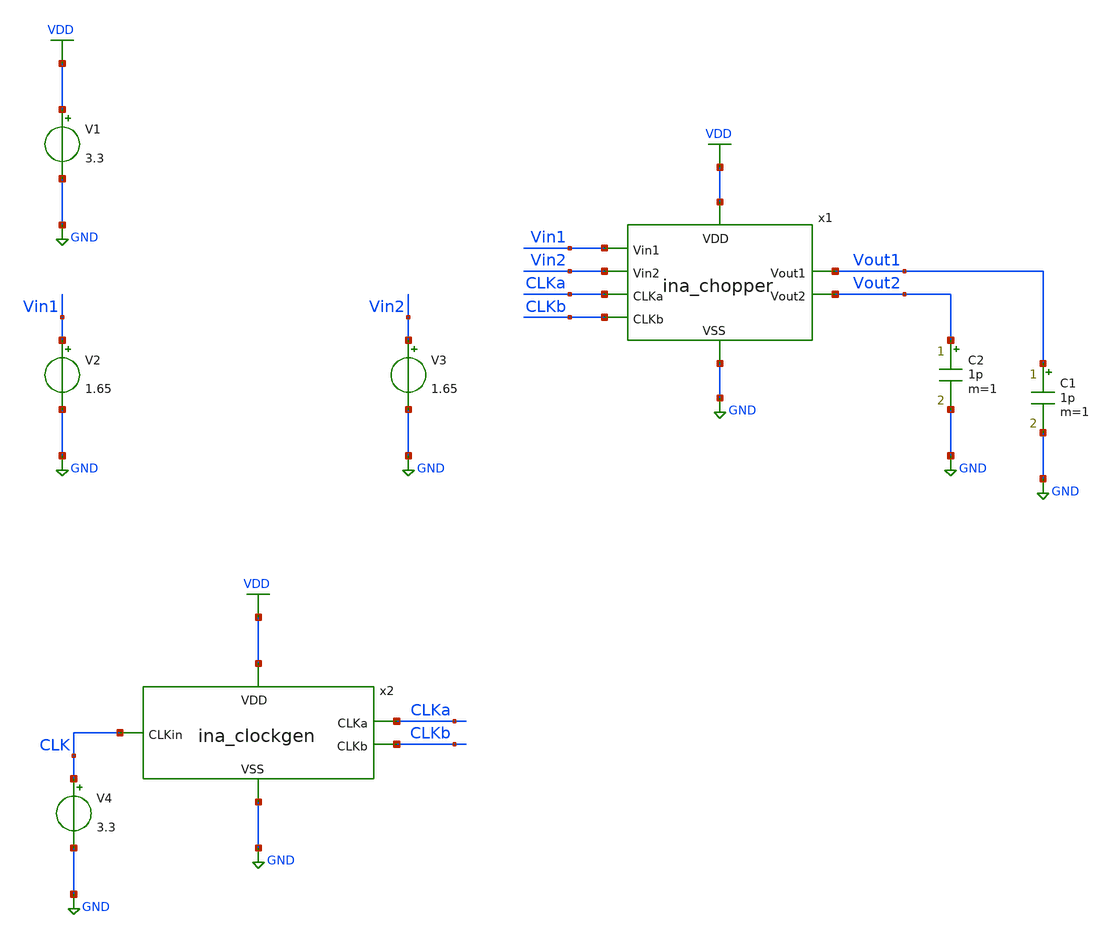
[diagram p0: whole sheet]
** sch_path: designs/libs/tb_ina/tb_ina_chopper_tran/tb_ina_chopper_tran.sch
**.subckt tb_ina_chopper_tran
V1 VDD GND 3.3
V2 Vin1 GND 1.65
V4 CLK GND 3.3
V3 Vin2 GND 1.65
C2 Vout2 GND 1p m=1
C1 Vout1 GND 1p m=1
x1 Vout2 Vin1 VDD GND CLKb CLKa Vout1 Vin2 ina_chopper
x2 VDD CLK CLKa CLKb GND ina_clockgen
**** begin user architecture code

.include $::180MCU_MODELS/design.ngspice
.lib $::180MCU_MODELS/sm141064.ngspice typical
.lib $::180MCU_MODELS/sm141064.ngspice cap_mim
.lib $::180MCU_MODELS/sm141064.ngspice moscap_typical
.lib $::180MCU_MODELS/sm141064.ngspice mimcap_typical
.lib $::180MCU_MODELS/sm141064.ngspice res_typical
* .lib $::180MCU_MODELS/sm141064.ngspice res_statistical
* ngspice commands




.control
save all

run
set color0 = white

*************************************
** ECG INPUT PARAMETERS
*************************************

let Vdd  = 3.3
let Vcm  = 1.65
let Vamp = 0.5m
let fecg = 100

*************************************
** CHOPPER PARAMETERS
*************************************

let fchop = 4k
let tper = 1/fchop
let ton = tper/2
let tr = 10n
let tf = 10n

*************************************
** TRANSIENT PARAMETERS
*************************************

let tstop = 10m
let tstep = 100n

*************************************
** SOURCES
*************************************

alter @V1[DC] = $&Vdd
alter @V2[SIN] = [ $&Vcm $&Vamp $&fecg ]
alter @V3[SIN] = [ $&Vcm -$&Vamp $&fecg ]
alter @V4[PULSE] = [ 0 $&Vdd 0 $&tr $&tf $&ton $&tper 0 ]

*************************************
** TRANSIENT SIMULATION
*************************************

tran $&tstep $&tstop

*************************************
** PLOTS
*************************************

setplot tran1
let vin_diff  = v(Vin1)-v(Vin2)
let vout_diff = v(Vout1)-v(Vout2)
let vin1 = v(Vin1)
let vin2 = v(Vin2)
let vout1 = v(Vout1)
let vout2 = v(Vout2)
let vclka = v(CLKa)
let vclkb = v(CLKb)
meas tran vmax1 MAX v(Vout1)
meas tran vmin1 MIN v(Vout1)
let spike = ((vmax1-vmin1)-1m)/2
plot vin_diff
plot vout_diff
plot vin1 vin2
plot vclka vclkb xlimit 0 500u
plot vout1 vout2
print spike

*************************************
** SAVE
*************************************

write tb_ina_chopper_tran.raw


.endc
* ngspice commands



**** end user architecture code
**.ends

* expanding   symbol:  libs/core_ina/ina_chopper/ina_chopper.sym # of pins=8
** sym_path: designs/libs/core_ina/ina_chopper/ina_chopper.sym
** sch_path: designs/libs/core_ina/ina_chopper/ina_chopper.sch
.subckt ina_chopper Vout2 Vin1 VDD VSS CLKb CLKa Vout1 Vin2
*.ipin Vin1
*.ipin Vin2
*.ipin CLKb
*.opin Vout2
*.ipin CLKa
*.opin Vout1
*.ipin VDD
*.ipin VSS
XM1 Vout1 CLKa Vin1 VSS nfet_03v3 L=0.28u W=2u nf=1 ad='int((nf+1)/2) * W/nf * 0.18u' as='int((nf+2)/2) * W/nf * 0.18u'
+ pd='2*int((nf+1)/2) * (W/nf + 0.18u)' ps='2*int((nf+2)/2) * (W/nf + 0.18u)' nrd='0.18u / W' nrs='0.18u / W'
+ sa=0 sb=0 sd=0 m=1
XM2 Vout1 CLKb Vin1 VDD pfet_03v3 L=0.28u W=2u nf=1 ad='int((nf+1)/2) * W/nf * 0.18u' as='int((nf+2)/2) * W/nf * 0.18u'
+ pd='2*int((nf+1)/2) * (W/nf + 0.18u)' ps='2*int((nf+2)/2) * (W/nf + 0.18u)' nrd='0.18u / W' nrs='0.18u / W'
+ sa=0 sb=0 sd=0 m=2
XM3 Vout2 CLKb Vin1 VSS nfet_03v3 L=0.28u W=2u nf=1 ad='int((nf+1)/2) * W/nf * 0.18u' as='int((nf+2)/2) * W/nf * 0.18u'
+ pd='2*int((nf+1)/2) * (W/nf + 0.18u)' ps='2*int((nf+2)/2) * (W/nf + 0.18u)' nrd='0.18u / W' nrs='0.18u / W'
+ sa=0 sb=0 sd=0 m=1
XM4 Vout2 CLKa Vin1 VDD pfet_03v3 L=0.28u W=2u nf=1 ad='int((nf+1)/2) * W/nf * 0.18u' as='int((nf+2)/2) * W/nf * 0.18u'
+ pd='2*int((nf+1)/2) * (W/nf + 0.18u)' ps='2*int((nf+2)/2) * (W/nf + 0.18u)' nrd='0.18u / W' nrs='0.18u / W'
+ sa=0 sb=0 sd=0 m=2
XM5 Vin2 CLKa Vout2 VSS nfet_03v3 L=0.28u W=2u nf=1 ad='int((nf+1)/2) * W/nf * 0.18u' as='int((nf+2)/2) * W/nf * 0.18u'
+ pd='2*int((nf+1)/2) * (W/nf + 0.18u)' ps='2*int((nf+2)/2) * (W/nf + 0.18u)' nrd='0.18u / W' nrs='0.18u / W'
+ sa=0 sb=0 sd=0 m=1
XM6 Vin2 CLKb Vout2 VDD pfet_03v3 L=0.28u W=2u nf=1 ad='int((nf+1)/2) * W/nf * 0.18u' as='int((nf+2)/2) * W/nf * 0.18u'
+ pd='2*int((nf+1)/2) * (W/nf + 0.18u)' ps='2*int((nf+2)/2) * (W/nf + 0.18u)' nrd='0.18u / W' nrs='0.18u / W'
+ sa=0 sb=0 sd=0 m=2
XM7 Vin2 CLKb Vout1 VSS nfet_03v3 L=0.28u W=2u nf=1 ad='int((nf+1)/2) * W/nf * 0.18u' as='int((nf+2)/2) * W/nf * 0.18u'
+ pd='2*int((nf+1)/2) * (W/nf + 0.18u)' ps='2*int((nf+2)/2) * (W/nf + 0.18u)' nrd='0.18u / W' nrs='0.18u / W'
+ sa=0 sb=0 sd=0 m=1
XM8 Vin2 CLKa Vout1 VDD pfet_03v3 L=0.28u W=2u nf=1 ad='int((nf+1)/2) * W/nf * 0.18u' as='int((nf+2)/2) * W/nf * 0.18u'
+ pd='2*int((nf+1)/2) * (W/nf + 0.18u)' ps='2*int((nf+2)/2) * (W/nf + 0.18u)' nrd='0.18u / W' nrs='0.18u / W'
+ sa=0 sb=0 sd=0 m=2
XM9 Vout1 CLKb Vout1 VSS nfet_03v3 L=0.28u W=1u nf=1 ad='int((nf+1)/2) * W/nf * 0.18u' as='int((nf+2)/2) * W/nf * 0.18u'
+ pd='2*int((nf+1)/2) * (W/nf + 0.18u)' ps='2*int((nf+2)/2) * (W/nf + 0.18u)' nrd='0.18u / W' nrs='0.18u / W'
+ sa=0 sb=0 sd=0 m=1
XM10 Vout1 CLKa Vout1 VDD pfet_03v3 L=0.28u W=1u nf=1 ad='int((nf+1)/2) * W/nf * 0.18u' as='int((nf+2)/2) * W/nf * 0.18u'
+ pd='2*int((nf+1)/2) * (W/nf + 0.18u)' ps='2*int((nf+2)/2) * (W/nf + 0.18u)' nrd='0.18u / W' nrs='0.18u / W'
+ sa=0 sb=0 sd=0 m=2
XM11 Vout2 CLKa Vout2 VSS nfet_03v3 L=0.28u W=1u nf=1 ad='int((nf+1)/2) * W/nf * 0.18u' as='int((nf+2)/2) * W/nf * 0.18u'
+ pd='2*int((nf+1)/2) * (W/nf + 0.18u)' ps='2*int((nf+2)/2) * (W/nf + 0.18u)' nrd='0.18u / W' nrs='0.18u / W'
+ sa=0 sb=0 sd=0 m=1
XM12 Vout2 CLKb Vout2 VDD pfet_03v3 L=0.28u W=1u nf=1 ad='int((nf+1)/2) * W/nf * 0.18u' as='int((nf+2)/2) * W/nf * 0.18u'
+ pd='2*int((nf+1)/2) * (W/nf + 0.18u)' ps='2*int((nf+2)/2) * (W/nf + 0.18u)' nrd='0.18u / W' nrs='0.18u / W'
+ sa=0 sb=0 sd=0 m=2
XM13 Vout2 CLKa Vout2 VDD pfet_03v3 L=0.28u W=1u nf=1 ad='int((nf+1)/2) * W/nf * 0.18u' as='int((nf+2)/2) * W/nf * 0.18u'
+ pd='2*int((nf+1)/2) * (W/nf + 0.18u)' ps='2*int((nf+2)/2) * (W/nf + 0.18u)' nrd='0.18u / W' nrs='0.18u / W'
+ sa=0 sb=0 sd=0 m=2
XM14 Vout2 CLKb Vout2 VSS nfet_03v3 L=0.28u W=1u nf=1 ad='int((nf+1)/2) * W/nf * 0.18u' as='int((nf+2)/2) * W/nf * 0.18u'
+ pd='2*int((nf+1)/2) * (W/nf + 0.18u)' ps='2*int((nf+2)/2) * (W/nf + 0.18u)' nrd='0.18u / W' nrs='0.18u / W'
+ sa=0 sb=0 sd=0 m=1
XM15 Vout1 CLKb Vout1 VDD pfet_03v3 L=0.28u W=1u nf=1 ad='int((nf+1)/2) * W/nf * 0.18u' as='int((nf+2)/2) * W/nf * 0.18u'
+ pd='2*int((nf+1)/2) * (W/nf + 0.18u)' ps='2*int((nf+2)/2) * (W/nf + 0.18u)' nrd='0.18u / W' nrs='0.18u / W'
+ sa=0 sb=0 sd=0 m=2
XM16 Vout1 CLKa Vout1 VSS nfet_03v3 L=0.28u W=1u nf=1 ad='int((nf+1)/2) * W/nf * 0.18u' as='int((nf+2)/2) * W/nf * 0.18u'
+ pd='2*int((nf+1)/2) * (W/nf + 0.18u)' ps='2*int((nf+2)/2) * (W/nf + 0.18u)' nrd='0.18u / W' nrs='0.18u / W'
+ sa=0 sb=0 sd=0 m=1
.ends


* expanding   symbol:  libs/core_ina/ina_clockgen/ina_clockgen.sym # of pins=5
** sym_path: designs/libs/core_ina/ina_clockgen/ina_clockgen.sym
** sch_path: designs/libs/core_ina/ina_clockgen/ina_clockgen.sch
.subckt ina_clockgen VDD CLKin CLKa CLKb VSS
*.ipin CLKin
*.ipin VDD
*.ipin VSS
*.opin CLKa
*.opin CLKb
x1 VDD net4 CLKin net1 VSS ina_nand
x2 VDD net6 net3 net2 VSS ina_nand
x3 VDD CLKin net2 VSS ina_inv
x4 VDD net4 net5 VSS ina_inv
x5 VDD net5 net3 VSS ina_inv
x6 VDD net3 CLKa VSS ina_inv
x7 VDD net6 net7 VSS ina_inv
x8 VDD net7 net1 VSS ina_inv
x9 VDD net1 CLKb VSS ina_inv
.ends


* expanding   symbol:  libs/core_ina/ina_nand/ina_nand.sym # of pins=5
** sym_path: designs/libs/core_ina/ina_nand/ina_nand.sym
** sch_path: designs/libs/core_ina/ina_nand/ina_nand.sch
.subckt ina_nand VDD Vout Vin1 Vin2 VSS
*.ipin VDD
*.ipin Vin1
*.ipin Vin2
*.ipin VSS
*.opin Vout
XMN1 Vout Vin1 VDD VDD pfet_03v3 L=0.28u W=2u nf=1 ad='int((nf+1)/2) * W/nf * 0.18u' as='int((nf+2)/2) * W/nf * 0.18u'
+ pd='2*int((nf+1)/2) * (W/nf + 0.18u)' ps='2*int((nf+2)/2) * (W/nf + 0.18u)' nrd='0.18u / W' nrs='0.18u / W'
+ sa=0 sb=0 sd=0 m=1
XMN2 Vout Vin2 VDD VDD pfet_03v3 L=0.28u W=2u nf=1 ad='int((nf+1)/2) * W/nf * 0.18u' as='int((nf+2)/2) * W/nf * 0.18u'
+ pd='2*int((nf+1)/2) * (W/nf + 0.18u)' ps='2*int((nf+2)/2) * (W/nf + 0.18u)' nrd='0.18u / W' nrs='0.18u / W'
+ sa=0 sb=0 sd=0 m=1
XMN3 Vout Vin1 net1 VSS nfet_03v3 L=0.28u W=2u nf=1 ad='int((nf+1)/2) * W/nf * 0.18u' as='int((nf+2)/2) * W/nf * 0.18u'
+ pd='2*int((nf+1)/2) * (W/nf + 0.18u)' ps='2*int((nf+2)/2) * (W/nf + 0.18u)' nrd='0.18u / W' nrs='0.18u / W'
+ sa=0 sb=0 sd=0 m=1
XMN4 net1 Vin2 VSS VSS nfet_03v3 L=0.28u W=2u nf=1 ad='int((nf+1)/2) * W/nf * 0.18u' as='int((nf+2)/2) * W/nf * 0.18u'
+ pd='2*int((nf+1)/2) * (W/nf + 0.18u)' ps='2*int((nf+2)/2) * (W/nf + 0.18u)' nrd='0.18u / W' nrs='0.18u / W'
+ sa=0 sb=0 sd=0 m=1
.ends


* expanding   symbol:  libs/core_ina/ina_inv/ina_inv.sym # of pins=4
** sym_path: designs/libs/core_ina/ina_inv/ina_inv.sym
** sch_path: designs/libs/core_ina/ina_inv/ina_inv.sch
.subckt ina_inv VDD Vin Vout VSS
*.ipin VDD
*.ipin VSS
*.ipin Vin
*.opin Vout
XMI1 Vout Vin VDD VDD pfet_03v3 L=0.28u W=2u nf=1 ad='int((nf+1)/2) * W/nf * 0.18u' as='int((nf+2)/2) * W/nf * 0.18u'
+ pd='2*int((nf+1)/2) * (W/nf + 0.18u)' ps='2*int((nf+2)/2) * (W/nf + 0.18u)' nrd='0.18u / W' nrs='0.18u / W'
+ sa=0 sb=0 sd=0 m=1
XMI2 Vout Vin VSS VSS nfet_03v3 L=0.28u W=1u nf=1 ad='int((nf+1)/2) * W/nf * 0.18u' as='int((nf+2)/2) * W/nf * 0.18u'
+ pd='2*int((nf+1)/2) * (W/nf + 0.18u)' ps='2*int((nf+2)/2) * (W/nf + 0.18u)' nrd='0.18u / W' nrs='0.18u / W'
+ sa=0 sb=0 sd=0 m=1
.ends

.GLOBAL GND
.GLOBAL VDD
.end
